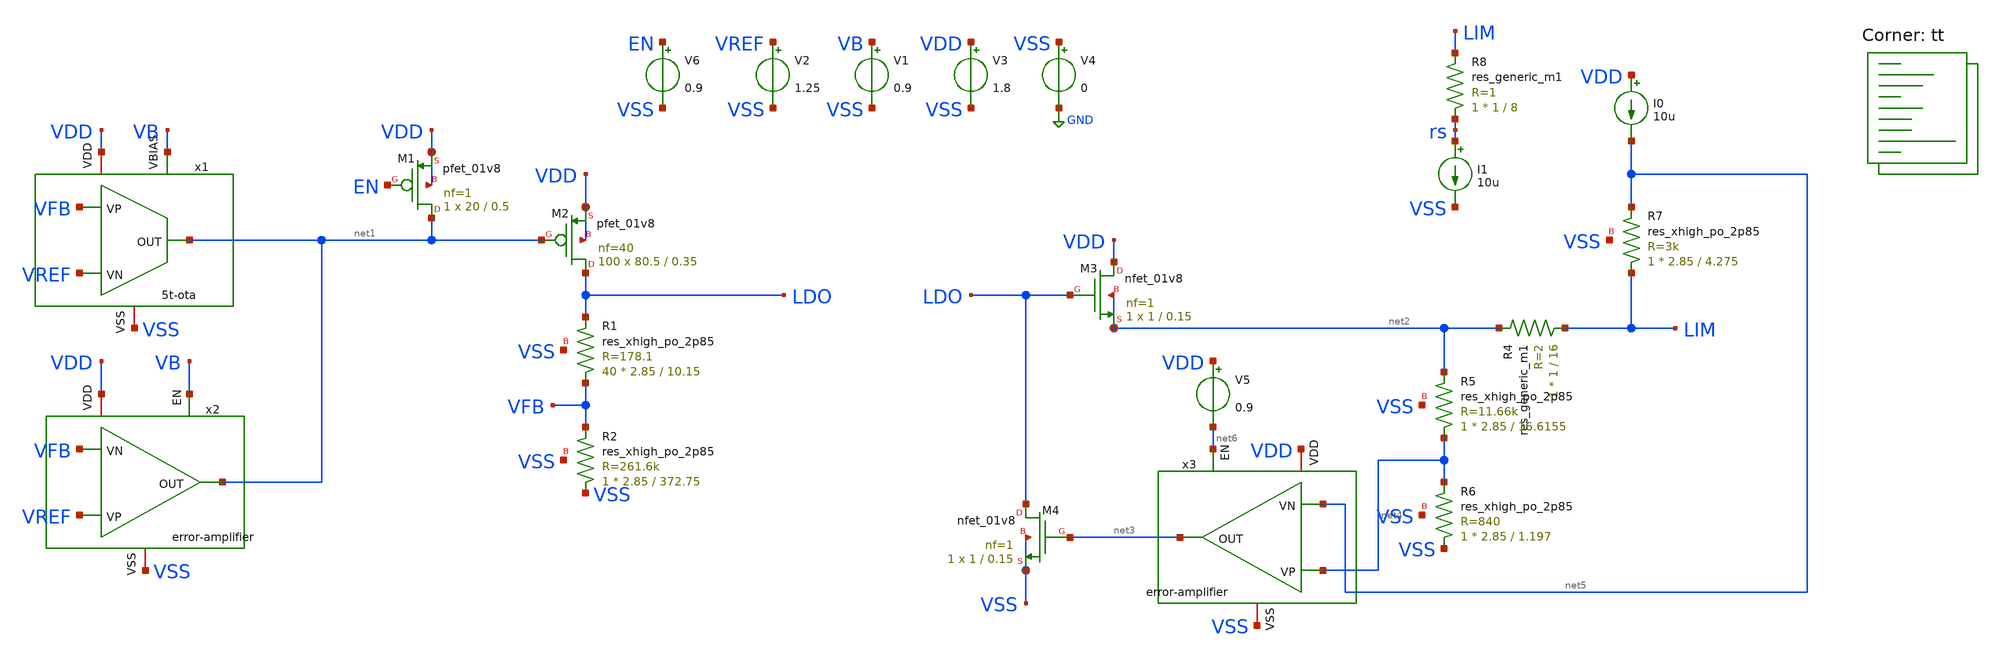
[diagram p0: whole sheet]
** sch_path: current_limit/current_limit.sch
**.subckt current_limit
x1 VDD net1 VFB VREF VB VSS 5t-ota
x2 VDD net1 VREF VFB VB VSS error-amplifier
XM1 net1 EN VDD VDD sky130_fd_pr__pfet_01v8 L=0.5 W=20 nf=1 ad='int((1 + 1)/2) * 20 / 1 * 0.29' as='int((1 + 2)/2) * 20 / 1 * 0.29'
+ pd='2*int((1 + 1)/2) * (20 / 1 + 0.29)' ps='2*int((1 + 2)/2) * (20 / 1 + 0.29)' nrd='0.29 / 20 ' nrs='0.29 / 20 '
+ sa=0 sb=0 sd=0 mult=1 m=1
XM2 LDO net1 VDD VDD sky130_fd_pr__pfet_01v8 L=0.35 W=80.5 nf=40 ad='int((40 + 1)/2) * 80.5 / 40 * 0.29'
+ as='int((40 + 2)/2) * 80.5 / 40 * 0.29' pd='2*int((40 + 1)/2) * (80.5 / 40 + 0.29)' ps='2*int((40 + 2)/2) * (80.5 / 40 + 0.29)'
+ nrd='0.29 / 80.5 ' nrs='0.29 / 80.5 ' sa=0 sb=0 sd=0 mult=100 m=100
XR1 VFB LDO VSS sky130_fd_pr__res_xhigh_po_2p85 L=10.15 mult=40 m=40
XR2 VSS VFB VSS sky130_fd_pr__res_xhigh_po_2p85 L=372.75 mult=1 m=1
x3 VDD net3 net4 net5 net6 VSS error-amplifier
XM3 VDD LDO net2 net2 sky130_fd_pr__nfet_01v8 L=0.15 W=1 nf=1 ad='int((1 + 1)/2) * 1 / 1 * 0.29' as='int((1 + 2)/2) * 1 / 1 * 0.29'
+ pd='2*int((1 + 1)/2) * (1 / 1 + 0.29)' ps='2*int((1 + 2)/2) * (1 / 1 + 0.29)' nrd='0.29 / 1 ' nrs='0.29 / 1 '
+ sa=0 sb=0 sd=0 mult=1 m=1
XM4 LDO net3 VSS VSS sky130_fd_pr__nfet_01v8 L=0.15 W=1 nf=1 ad='int((1 + 1)/2) * 1 / 1 * 0.29' as='int((1 + 2)/2) * 1 / 1 * 0.29'
+ pd='2*int((1 + 1)/2) * (1 / 1 + 0.29)' ps='2*int((1 + 2)/2) * (1 / 1 + 0.29)' nrd='0.29 / 1 ' nrs='0.29 / 1 '
+ sa=0 sb=0 sd=0 mult=1 m=1
R4 LIM net2 sky130_fd_pr__res_generic_m1 W=1 L=16 m=1
XR5 net4 net2 VSS sky130_fd_pr__res_xhigh_po_2p85 L=16.6155 mult=1 m=1
XR6 VSS net4 VSS sky130_fd_pr__res_xhigh_po_2p85 L=1.197 mult=1 m=1
XR7 LIM net5 VSS sky130_fd_pr__res_xhigh_po_2p85 L=4.275 mult=1 m=1
I0 VDD net5 10u
V3 VDD VSS 1.8
V4 VSS GND 0
I1 rs VSS 10u
V5 VDD net6 0.9
R8 rs LIM sky130_fd_pr__res_generic_m1 W=1 L=8 m=1
V1 VB VSS 0.9
V2 VREF VSS 1.25
V6 EN VSS 0.9
**** begin user architecture code
.lib $::SKYWATER_MODELS/sky130.lib.spice tt


.control
save all
set noaskquit

* Sweep load current
dc I1 0 500m 2m

* Load current via Rsense (1 ohm)
plot v(lim,rs)

* The foldback verdict plot
plot v(lim) vs v(lim,rs)

.endc



**** end user architecture code
**.ends
.GLOBAL GND
.end
